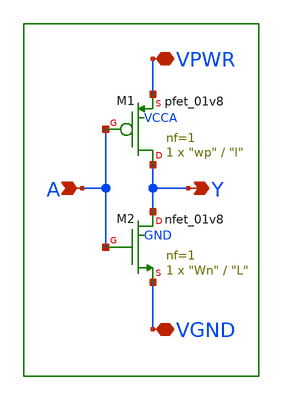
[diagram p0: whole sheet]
** sch_path: xschem/lib/aux_inv.sch
**.subckt aux_inv VPWR VGND A Y
*.iopin VPWR
*.iopin VGND
*.ipin A
*.opin Y
XM1 Y A VPWR VCCA sky130_fd_pr__pfet_01v8 L="l" W="wp" nf=1 ad='int((1 + 1)/2) * "wp" / 1 * 0.29' as='int((1 + 2)/2) * "wp" / 1 * 0.29'
+ pd='2*int((1 + 1)/2) * ("wp" / 1 + 0.29)' ps='2*int((1 + 2)/2) * ("wp" / 1 + 0.29)' nrd='0.29 / "wp" '
+ nrs='0.29 / "wp" ' sa=0 sb=0 sd=0 mult=1 m=1
XM2 Y A VGND GND sky130_fd_pr__nfet_01v8 L="L" W="Wn" nf=1 ad='int((nf+1)/2) * W/nf * 0.29' as='int((nf+2)/2) * W/nf * 0.29'
+ pd='2*int((nf+1)/2) * (W/nf + 0.29)' ps='2*int((nf+2)/2) * (W/nf + 0.29)' nrd='0.29 / W' nrs='0.29 / W'
+ sa=0 sb=0 sd=0 mult=1 m=1
**.ends
.end
